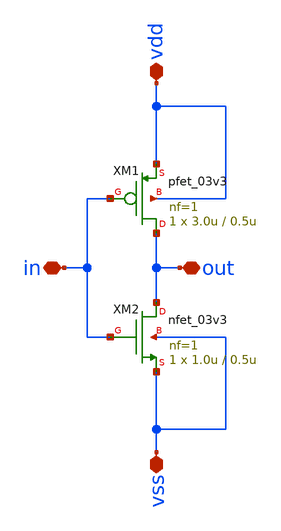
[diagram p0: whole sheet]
** sch_path: designs/libs/core_analog/inv1u05u/inv1u05u.sch
**.subckt inv1u05u in out vss vdd
*.iopin in
*.iopin out
*.iopin vss
*.iopin vdd
XM1 out in vdd vdd pfet_03v3 L=0.5u W=3.0u nf=1 ad='int((nf+1)/2) * W/nf * 0.18u' as='int((nf+2)/2) * W/nf * 0.18u'
+ pd='2*int((nf+1)/2) * (W/nf + 0.18u)' ps='2*int((nf+2)/2) * (W/nf + 0.18u)' nrd='0.18u / W' nrs='0.18u / W'
+ sa=0 sb=0 sd=0 m=1
XM2 out in vss vss nfet_03v3 L=0.5u W=1.0u nf=1 ad='int((nf+1)/2) * W/nf * 0.18u' as='int((nf+2)/2) * W/nf * 0.18u'
+ pd='2*int((nf+1)/2) * (W/nf + 0.18u)' ps='2*int((nf+2)/2) * (W/nf + 0.18u)' nrd='0.18u / W' nrs='0.18u / W'
+ sa=0 sb=0 sd=0 m=1
**.ends
.end
